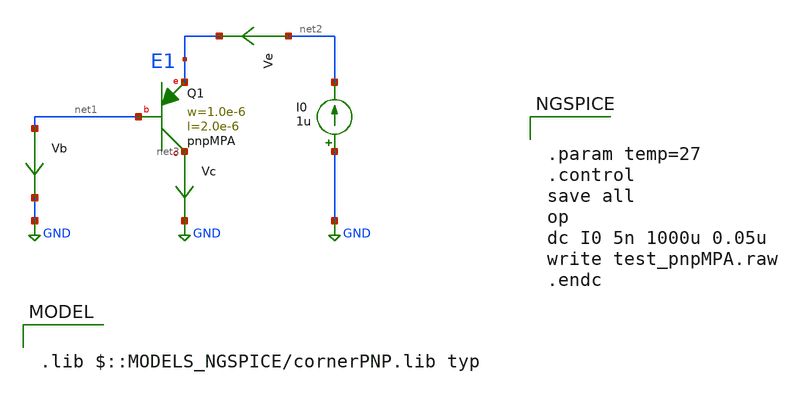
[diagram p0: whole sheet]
** sch_path: ihp-sg13cmos5l/libs.tech/xschem/tests/dc_pnpMPA.sch
* Copyright 2023 IHP PDK Authors
**.subckt dc_pnpMPA
Ve net2 E1 0
.save i(ve)
Vb net1 GND 0
.save i(vb)
Vc net3 GND 0
.save i(vc)
I0 GND net2 1u
XQ1 net3 net1 E1 pnpMPA a=2p p=6u m=1
**** begin user architecture code

.lib $::MODELS_NGSPICE/cornerPNP.lib typ



.param temp=27
.control
save all
op
dc I0 5n 1000u 0.05u
write test_pnpMPA.raw
.endc


**** end user architecture code
**.ends
.GLOBAL GND
.end
